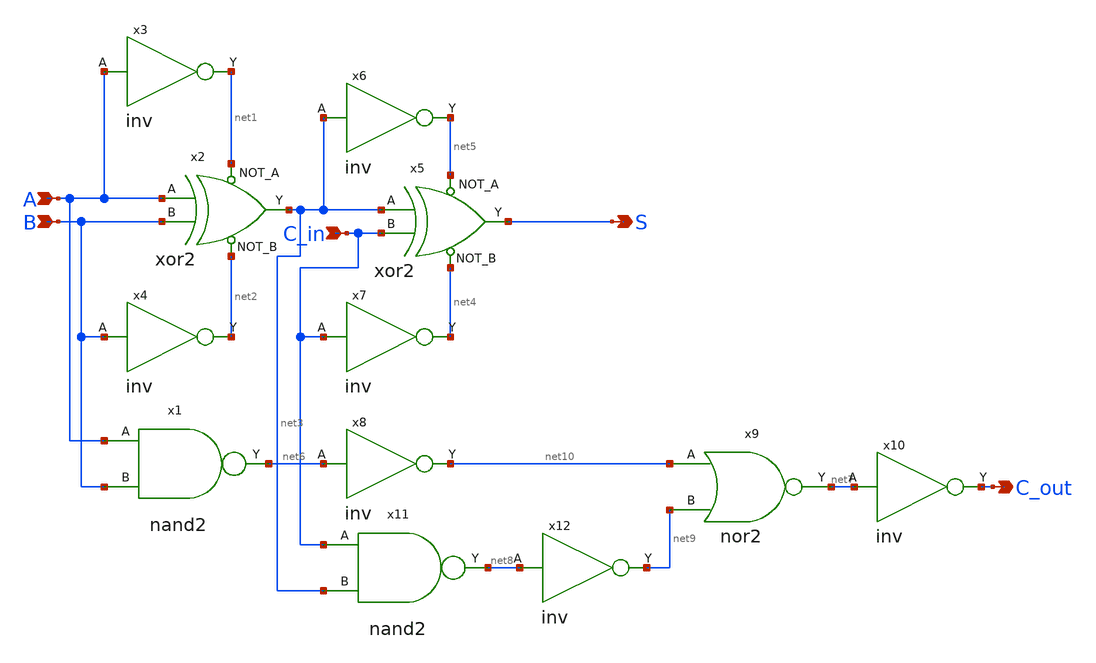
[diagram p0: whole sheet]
** sch_path: library/xschem/full_adder_components.sch
**.subckt full_adder_components S A B C_in C_out
*.opin S
*.ipin A
*.ipin B
*.ipin C_in
*.opin C_out
x2 A B net1 net2 net3 xor2
x3 A net1 inv
x4 B net2 inv
x5 net3 C_in net5 net4 S xor2
x6 net3 net5 inv
x7 C_in net4 inv
x1 A net6 B nand2
x8 net6 net10 inv
x9 net10 net9 net7 nor2
x10 net7 C_out inv
x11 C_in net8 net3 nand2
x12 net8 net9 inv
**.ends

* expanding   symbol:  xor2.sym # of pins=5
** sym_path: library/xschem/xor2.sym
** sch_path: library/xschem/xor2.sch
.subckt xor2 A B NOT_A NOT_B Y
*.opin Y
*.ipin A
*.ipin B
*.ipin NOT_A
*.ipin NOT_B
XM1 Y NOT_B net2 GND sky130_fd_pr__nfet_01v8 L=0.15 W=1 nf=1 ad='int((nf+1)/2) * W/nf * 0.29' as='int((nf+2)/2) * W/nf * 0.29'
+ pd='2*int((nf+1)/2) * (W/nf + 0.29)' ps='2*int((nf+2)/2) * (W/nf + 0.29)' nrd='0.29 / W' nrs='0.29 / W'
+ sa=0 sb=0 sd=0 mult=1 m=1
XM2 net1 A VDD VDD sky130_fd_pr__pfet_01v8 L=0.15 W=1 nf=1 ad='int((nf+1)/2) * W/nf * 0.29' as='int((nf+2)/2) * W/nf * 0.29'
+ pd='2*int((nf+1)/2) * (W/nf + 0.29)' ps='2*int((nf+2)/2) * (W/nf + 0.29)' nrd='0.29 / W' nrs='0.29 / W'
+ sa=0 sb=0 sd=0 mult=1 m=1
XM4 net2 NOT_A GND GND sky130_fd_pr__nfet_01v8 L=0.15 W=1 nf=1 ad='int((nf+1)/2) * W/nf * 0.29' as='int((nf+2)/2) * W/nf * 0.29'
+ pd='2*int((nf+1)/2) * (W/nf + 0.29)' ps='2*int((nf+2)/2) * (W/nf + 0.29)' nrd='0.29 / W' nrs='0.29 / W'
+ sa=0 sb=0 sd=0 mult=1 m=1
XM3 net1 B VDD VDD sky130_fd_pr__pfet_01v8 L=0.15 W=1 nf=1 ad='int((nf+1)/2) * W/nf * 0.29' as='int((nf+2)/2) * W/nf * 0.29'
+ pd='2*int((nf+1)/2) * (W/nf + 0.29)' ps='2*int((nf+2)/2) * (W/nf + 0.29)' nrd='0.29 / W' nrs='0.29 / W'
+ sa=0 sb=0 sd=0 mult=1 m=1
XM5 Y NOT_B net1 VDD sky130_fd_pr__pfet_01v8 L=0.15 W=1 nf=1 ad='int((nf+1)/2) * W/nf * 0.29' as='int((nf+2)/2) * W/nf * 0.29'
+ pd='2*int((nf+1)/2) * (W/nf + 0.29)' ps='2*int((nf+2)/2) * (W/nf + 0.29)' nrd='0.29 / W' nrs='0.29 / W'
+ sa=0 sb=0 sd=0 mult=1 m=1
XM6 Y NOT_A net1 VDD sky130_fd_pr__pfet_01v8 L=0.15 W=1 nf=1 ad='int((nf+1)/2) * W/nf * 0.29' as='int((nf+2)/2) * W/nf * 0.29'
+ pd='2*int((nf+1)/2) * (W/nf + 0.29)' ps='2*int((nf+2)/2) * (W/nf + 0.29)' nrd='0.29 / W' nrs='0.29 / W'
+ sa=0 sb=0 sd=0 mult=1 m=1
XM7 Y A net3 GND sky130_fd_pr__nfet_01v8 L=0.15 W=1 nf=1 ad='int((nf+1)/2) * W/nf * 0.29' as='int((nf+2)/2) * W/nf * 0.29'
+ pd='2*int((nf+1)/2) * (W/nf + 0.29)' ps='2*int((nf+2)/2) * (W/nf + 0.29)' nrd='0.29 / W' nrs='0.29 / W'
+ sa=0 sb=0 sd=0 mult=1 m=1
XM8 net3 B GND GND sky130_fd_pr__nfet_01v8 L=0.15 W=1 nf=1 ad='int((nf+1)/2) * W/nf * 0.29' as='int((nf+2)/2) * W/nf * 0.29'
+ pd='2*int((nf+1)/2) * (W/nf + 0.29)' ps='2*int((nf+2)/2) * (W/nf + 0.29)' nrd='0.29 / W' nrs='0.29 / W'
+ sa=0 sb=0 sd=0 mult=1 m=1
.ends


* expanding   symbol:  inv.sym # of pins=2
** sym_path: library/xschem/inv.sym
** sch_path: library/xschem/inv.sch
.subckt inv A Y
*.opin Y
*.ipin A
XM1 Y A GND GND sky130_fd_pr__nfet_01v8 L=0.15 W=1 nf=1 ad='int((nf+1)/2) * W/nf * 0.29' as='int((nf+2)/2) * W/nf * 0.29'
+ pd='2*int((nf+1)/2) * (W/nf + 0.29)' ps='2*int((nf+2)/2) * (W/nf + 0.29)' nrd='0.29 / W' nrs='0.29 / W'
+ sa=0 sb=0 sd=0 mult=1 m=1
XM2 Y A VDD VDD sky130_fd_pr__pfet_01v8 L=0.15 W=1 nf=1 ad='int((nf+1)/2) * W/nf * 0.29' as='int((nf+2)/2) * W/nf * 0.29'
+ pd='2*int((nf+1)/2) * (W/nf + 0.29)' ps='2*int((nf+2)/2) * (W/nf + 0.29)' nrd='0.29 / W' nrs='0.29 / W'
+ sa=0 sb=0 sd=0 mult=1 m=1
.ends


* expanding   symbol:  nand2.sym # of pins=3
** sym_path: library/xschem/nand2.sym
** sch_path: library/xschem/nand2.sch
.subckt nand2 A Y B
*.opin Y
*.ipin A
*.ipin B
XM1 Y B net1 GND sky130_fd_pr__nfet_01v8 L=0.15 W=1 nf=1 ad='int((nf+1)/2) * W/nf * 0.29' as='int((nf+2)/2) * W/nf * 0.29'
+ pd='2*int((nf+1)/2) * (W/nf + 0.29)' ps='2*int((nf+2)/2) * (W/nf + 0.29)' nrd='0.29 / W' nrs='0.29 / W'
+ sa=0 sb=0 sd=0 mult=1 m=1
XM2 Y B VDD VDD sky130_fd_pr__pfet_01v8 L=0.15 W=1 nf=1 ad='int((nf+1)/2) * W/nf * 0.29' as='int((nf+2)/2) * W/nf * 0.29'
+ pd='2*int((nf+1)/2) * (W/nf + 0.29)' ps='2*int((nf+2)/2) * (W/nf + 0.29)' nrd='0.29 / W' nrs='0.29 / W'
+ sa=0 sb=0 sd=0 mult=1 m=1
XM3 Y A VDD VDD sky130_fd_pr__pfet_01v8 L=0.15 W=1 nf=1 ad='int((nf+1)/2) * W/nf * 0.29' as='int((nf+2)/2) * W/nf * 0.29'
+ pd='2*int((nf+1)/2) * (W/nf + 0.29)' ps='2*int((nf+2)/2) * (W/nf + 0.29)' nrd='0.29 / W' nrs='0.29 / W'
+ sa=0 sb=0 sd=0 mult=1 m=1
XM4 net1 A GND GND sky130_fd_pr__nfet_01v8 L=0.15 W=1 nf=1 ad='int((nf+1)/2) * W/nf * 0.29' as='int((nf+2)/2) * W/nf * 0.29'
+ pd='2*int((nf+1)/2) * (W/nf + 0.29)' ps='2*int((nf+2)/2) * (W/nf + 0.29)' nrd='0.29 / W' nrs='0.29 / W'
+ sa=0 sb=0 sd=0 mult=1 m=1
.ends


* expanding   symbol:  nor2.sym # of pins=3
** sym_path: library/xschem/nor2.sym
** sch_path: library/xschem/nor2.sch
.subckt nor2 A B Y
*.opin Y
*.ipin A
*.ipin B
XM1 Y B GND GND sky130_fd_pr__nfet_01v8 L=0.15 W=1 nf=1 ad='int((nf+1)/2) * W/nf * 0.29' as='int((nf+2)/2) * W/nf * 0.29'
+ pd='2*int((nf+1)/2) * (W/nf + 0.29)' ps='2*int((nf+2)/2) * (W/nf + 0.29)' nrd='0.29 / W' nrs='0.29 / W'
+ sa=0 sb=0 sd=0 mult=1 m=1
XM2 Y B net1 VDD sky130_fd_pr__pfet_01v8 L=0.15 W=1 nf=1 ad='int((nf+1)/2) * W/nf * 0.29' as='int((nf+2)/2) * W/nf * 0.29'
+ pd='2*int((nf+1)/2) * (W/nf + 0.29)' ps='2*int((nf+2)/2) * (W/nf + 0.29)' nrd='0.29 / W' nrs='0.29 / W'
+ sa=0 sb=0 sd=0 mult=1 m=1
XM3 net1 A VDD VDD sky130_fd_pr__pfet_01v8 L=0.15 W=1 nf=1 ad='int((nf+1)/2) * W/nf * 0.29' as='int((nf+2)/2) * W/nf * 0.29'
+ pd='2*int((nf+1)/2) * (W/nf + 0.29)' ps='2*int((nf+2)/2) * (W/nf + 0.29)' nrd='0.29 / W' nrs='0.29 / W'
+ sa=0 sb=0 sd=0 mult=1 m=1
XM4 Y A GND GND sky130_fd_pr__nfet_01v8 L=0.15 W=1 nf=1 ad='int((nf+1)/2) * W/nf * 0.29' as='int((nf+2)/2) * W/nf * 0.29'
+ pd='2*int((nf+1)/2) * (W/nf + 0.29)' ps='2*int((nf+2)/2) * (W/nf + 0.29)' nrd='0.29 / W' nrs='0.29 / W'
+ sa=0 sb=0 sd=0 mult=1 m=1
.ends

.GLOBAL VDD
.GLOBAL GND
.end
